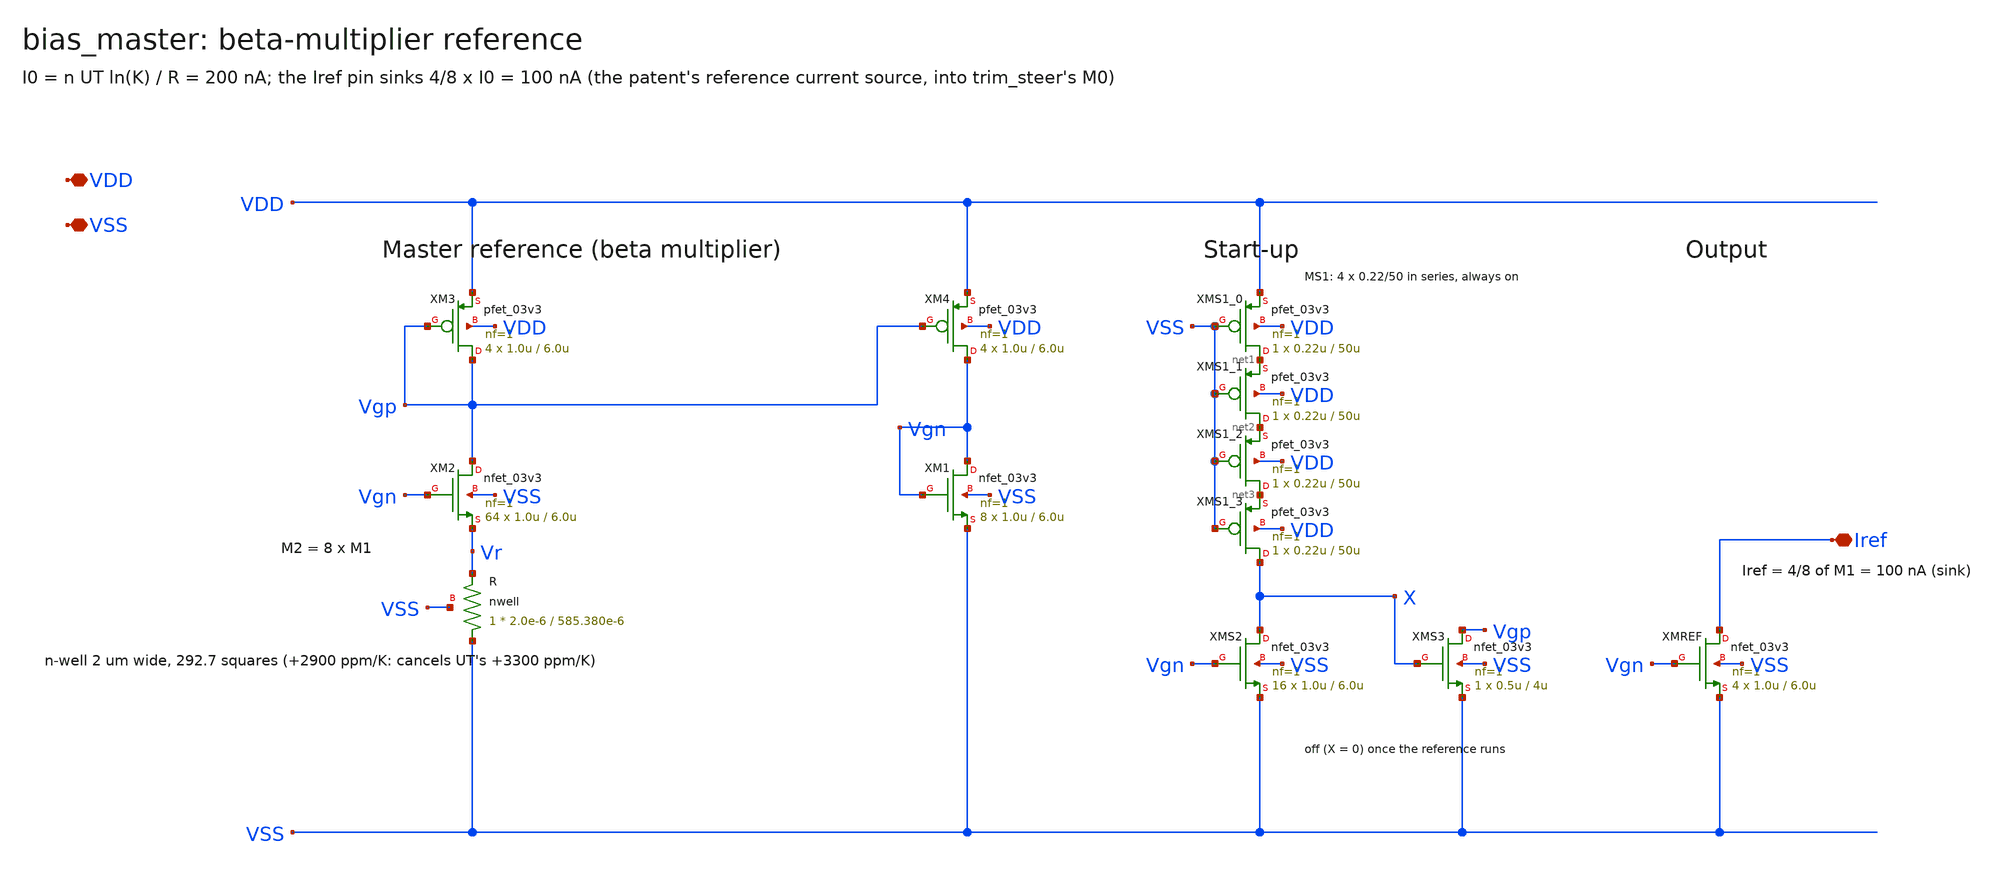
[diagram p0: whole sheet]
** sch_path: analog/bias/generator/bias_master.sch
**.subckt bias_master VDD VSS Iref
*.iopin VDD
*.iopin VSS
*.iopin Iref
XM3 Vgp Vgp VDD VDD pfet_03v3 L=6.0u W=1.0u nf=1 ad='int((nf+1)/2) * W/nf * 0.18u' as='int((nf+2)/2) * W/nf * 0.18u'
+ pd='2*int((nf+1)/2) * (W/nf + 0.18u)' ps='2*int((nf+2)/2) * (W/nf + 0.18u)' nrd='0.18u / W' nrs='0.18u / W'
+ sa=0 sb=0 sd=0 m=4
XM4 Vgn Vgp VDD VDD pfet_03v3 L=6.0u W=1.0u nf=1 ad='int((nf+1)/2) * W/nf * 0.18u' as='int((nf+2)/2) * W/nf * 0.18u'
+ pd='2*int((nf+1)/2) * (W/nf + 0.18u)' ps='2*int((nf+2)/2) * (W/nf + 0.18u)' nrd='0.18u / W' nrs='0.18u / W'
+ sa=0 sb=0 sd=0 m=4
XM2 Vgp Vgn Vr VSS nfet_03v3 L=6.0u W=1.0u nf=1 ad='int((nf+1)/2) * W/nf * 0.18u' as='int((nf+2)/2) * W/nf * 0.18u'
+ pd='2*int((nf+1)/2) * (W/nf + 0.18u)' ps='2*int((nf+2)/2) * (W/nf + 0.18u)' nrd='0.18u / W' nrs='0.18u / W'
+ sa=0 sb=0 sd=0 m=64
XM1 Vgn Vgn VSS VSS nfet_03v3 L=6.0u W=1.0u nf=1 ad='int((nf+1)/2) * W/nf * 0.18u' as='int((nf+2)/2) * W/nf * 0.18u'
+ pd='2*int((nf+1)/2) * (W/nf + 0.18u)' ps='2*int((nf+2)/2) * (W/nf + 0.18u)' nrd='0.18u / W' nrs='0.18u / W'
+ sa=0 sb=0 sd=0 m=8
XR VSS Vr VSS nwell r_width=2.0e-6 r_length=585.380e-6 m=1
XMS1_0 net1 VSS VDD VDD pfet_03v3 L=50u W=0.22u nf=1 ad='int((nf+1)/2) * W/nf * 0.18u' as='int((nf+2)/2) * W/nf * 0.18u'
+ pd='2*int((nf+1)/2) * (W/nf + 0.18u)' ps='2*int((nf+2)/2) * (W/nf + 0.18u)' nrd='0.18u / W' nrs='0.18u / W'
+ sa=0 sb=0 sd=0 m=1
XMS1_1 net2 VSS net1 VDD pfet_03v3 L=50u W=0.22u nf=1 ad='int((nf+1)/2) * W/nf * 0.18u' as='int((nf+2)/2) * W/nf * 0.18u'
+ pd='2*int((nf+1)/2) * (W/nf + 0.18u)' ps='2*int((nf+2)/2) * (W/nf + 0.18u)' nrd='0.18u / W' nrs='0.18u / W'
+ sa=0 sb=0 sd=0 m=1
XMS1_2 net3 VSS net2 VDD pfet_03v3 L=50u W=0.22u nf=1 ad='int((nf+1)/2) * W/nf * 0.18u' as='int((nf+2)/2) * W/nf * 0.18u'
+ pd='2*int((nf+1)/2) * (W/nf + 0.18u)' ps='2*int((nf+2)/2) * (W/nf + 0.18u)' nrd='0.18u / W' nrs='0.18u / W'
+ sa=0 sb=0 sd=0 m=1
XMS1_3 X VSS net3 VDD pfet_03v3 L=50u W=0.22u nf=1 ad='int((nf+1)/2) * W/nf * 0.18u' as='int((nf+2)/2) * W/nf * 0.18u'
+ pd='2*int((nf+1)/2) * (W/nf + 0.18u)' ps='2*int((nf+2)/2) * (W/nf + 0.18u)' nrd='0.18u / W' nrs='0.18u / W'
+ sa=0 sb=0 sd=0 m=1
XMS2 X Vgn VSS VSS nfet_03v3 L=6.0u W=1.0u nf=1 ad='int((nf+1)/2) * W/nf * 0.18u' as='int((nf+2)/2) * W/nf * 0.18u'
+ pd='2*int((nf+1)/2) * (W/nf + 0.18u)' ps='2*int((nf+2)/2) * (W/nf + 0.18u)' nrd='0.18u / W' nrs='0.18u / W'
+ sa=0 sb=0 sd=0 m=16
XMS3 Vgp X VSS VSS nfet_03v3 L=4u W=0.5u nf=1 ad='int((nf+1)/2) * W/nf * 0.18u' as='int((nf+2)/2) * W/nf * 0.18u'
+ pd='2*int((nf+1)/2) * (W/nf + 0.18u)' ps='2*int((nf+2)/2) * (W/nf + 0.18u)' nrd='0.18u / W' nrs='0.18u / W'
+ sa=0 sb=0 sd=0 m=1
XMREF Iref Vgn VSS VSS nfet_03v3 L=6.0u W=1.0u nf=1 ad='int((nf+1)/2) * W/nf * 0.18u' as='int((nf+2)/2) * W/nf * 0.18u'
+ pd='2*int((nf+1)/2) * (W/nf + 0.18u)' ps='2*int((nf+2)/2) * (W/nf + 0.18u)' nrd='0.18u / W' nrs='0.18u / W'
+ sa=0 sb=0 sd=0 m=4
**.ends
.end
